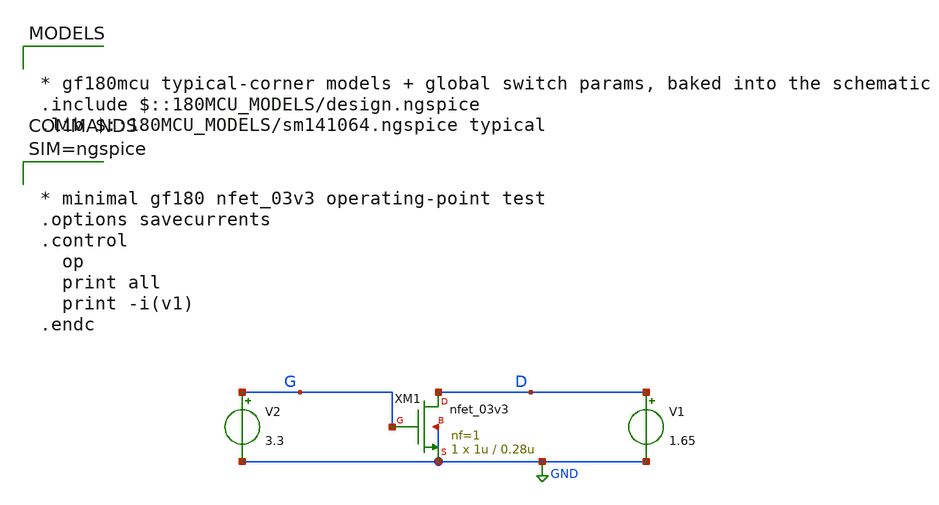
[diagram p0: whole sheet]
** sch_path: gf180mcuD/xschem_libs/gf180mcu_tests/nfet_test_claude/schematic/nfet_test_claude.sch
**.subckt nfet_test_claude
XM1 D G GND GND nfet_03v3 L=0.28u W=1u nf=1 ad='int((nf+1)/2) * W/nf * 0.18u' as='int((nf+2)/2) * W/nf * 0.18u'
+ pd='2*int((nf+1)/2) * (W/nf + 0.18u)' ps='2*int((nf+2)/2) * (W/nf + 0.18u)' nrd='0.18u / W' nrs='0.18u / W'
+ sa=0 sb=0 sd=0 m=1
V1 D GND 1.65
V2 G GND 3.3
**** begin user architecture code

* gf180mcu typical-corner models + global switch params, baked into the schematic
.include $::180MCU_MODELS/design.ngspice
.lib $::180MCU_MODELS/sm141064.ngspice typical




* minimal gf180 nfet_03v3 operating-point test
.options savecurrents
.control
  op
  print all
  print -i(v1)
.endc



**** end user architecture code
**.ends
.GLOBAL GND
.end
